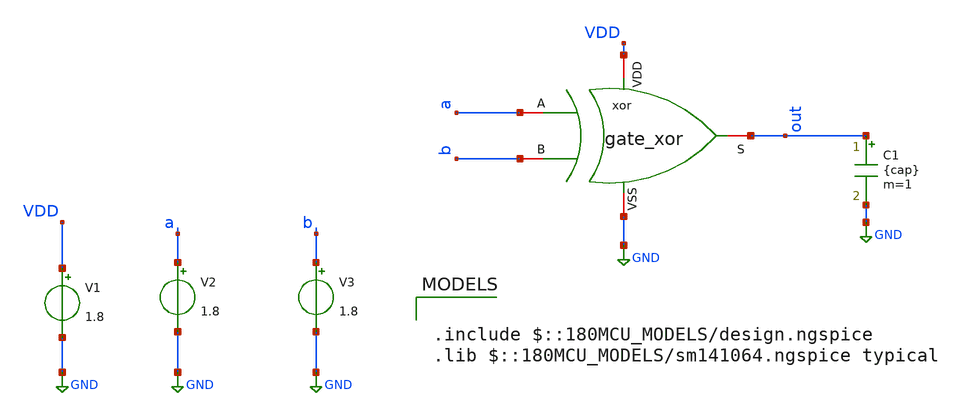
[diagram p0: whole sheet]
** sch_path: designs/DS_modulator/gate_xor/xschem/gate_xor_TB.sch
**.subckt gate_xor_TB
V1 VDD GND 1.8
V2 a GND 1.8
V3 b GND 1.8
xor VDD out a b GND gate_xor
C1 out GND {cap} m=1
**** begin user architecture code

.include $::180MCU_MODELS/design.ngspice
.lib $::180MCU_MODELS/sm141064.ngspice typical




.control
*------------------- Parámetros -------------------
.param wxor=5.6u
.param cap=5f

*------------------- Guardar nodos -------------------
save all

* Entradas A y B con pulsos desfasados
alter @v2[PULSE]=(0 1.8 0 10p 10p 2.5n 10n)   ; Señal A
alter @v3[PULSE]=(0 1.8 0 10p 10p 1.5n 5n)    ; Señal B

*------------------- Simulación -------------------
TRAN 0.01n 20n


plot v(A) v(B) v(out)


* Medidas para caracterización
.meas TRAN t_rise TRIG v(b)=0.9 RISE=1 TARG v(out)=0.9 RISE=1
.meas TRAN t_fall TRIG v(b)=0.9 FALL=1 TARG v(out)=0.9 FALL=1

* Guardar resultados
*write prueba_xor.raw
.endc


**** end user architecture code
**.ends

* expanding   symbol:  gf180/gate_xor/xschem/gate_xor.sym # of pins=5
** sym_path: designs/DS_modulator/gate_xor/xschem/gate_xor.sym
** sch_path: designs/DS_modulator/gate_xor/xschem/gate_xor.sch
.subckt gate_xor VDD S A B VSS
*.iopin VSS
*.iopin VDD
*.iopin S
*.iopin A
*.iopin B
XM2 S B vz VSS nfet_03v3 L=0.28u W=1u nf=1 ad='int((nf+1)/2) * W/nf * 0.18u' as='int((nf+2)/2) * W/nf * 0.18u'
+ pd='2*int((nf+1)/2) * (W/nf + 0.18u)' ps='2*int((nf+2)/2) * (W/nf + 0.18u)' nrd='0.18u / W' nrs='0.18u / W'
+ sa=0 sb=0 sd=0 m=4
XM3 S -B vx VDD pfet_03v3 L=0.28u W=3u nf=1 ad='int((nf+1)/2) * W/nf * 0.18u' as='int((nf+2)/2) * W/nf * 0.18u'
+ pd='2*int((nf+1)/2) * (W/nf + 0.18u)' ps='2*int((nf+2)/2) * (W/nf + 0.18u)' nrd='0.18u / W' nrs='0.18u / W'
+ sa=0 sb=0 sd=0 m=4
XM1 vx A VDD VDD pfet_03v3 L=0.28u W=3u nf=1 ad='int((nf+1)/2) * W/nf * 0.18u' as='int((nf+2)/2) * W/nf * 0.18u'
+ pd='2*int((nf+1)/2) * (W/nf + 0.18u)' ps='2*int((nf+2)/2) * (W/nf + 0.18u)' nrd='0.18u / W' nrs='0.18u / W'
+ sa=0 sb=0 sd=0 m=4
XM4 S -B vw VSS nfet_03v3 L=0.28u W=1u nf=1 ad='int((nf+1)/2) * W/nf * 0.18u' as='int((nf+2)/2) * W/nf * 0.18u'
+ pd='2*int((nf+1)/2) * (W/nf + 0.18u)' ps='2*int((nf+2)/2) * (W/nf + 0.18u)' nrd='0.18u / W' nrs='0.18u / W'
+ sa=0 sb=0 sd=0 m=4
XM5 S B vy VDD pfet_03v3 L=0.28u W=3u nf=1 ad='int((nf+1)/2) * W/nf * 0.18u' as='int((nf+2)/2) * W/nf * 0.18u'
+ pd='2*int((nf+1)/2) * (W/nf + 0.18u)' ps='2*int((nf+2)/2) * (W/nf + 0.18u)' nrd='0.18u / W' nrs='0.18u / W'
+ sa=0 sb=0 sd=0 m=4
XM6 vy -A VDD VDD pfet_03v3 L=0.28u W=3u nf=1 ad='int((nf+1)/2) * W/nf * 0.18u' as='int((nf+2)/2) * W/nf * 0.18u'
+ pd='2*int((nf+1)/2) * (W/nf + 0.18u)' ps='2*int((nf+2)/2) * (W/nf + 0.18u)' nrd='0.18u / W' nrs='0.18u / W'
+ sa=0 sb=0 sd=0 m=4
XM7 vz A VSS VSS nfet_03v3 L=0.28u W=1u nf=1 ad='int((nf+1)/2) * W/nf * 0.18u' as='int((nf+2)/2) * W/nf * 0.18u'
+ pd='2*int((nf+1)/2) * (W/nf + 0.18u)' ps='2*int((nf+2)/2) * (W/nf + 0.18u)' nrd='0.18u / W' nrs='0.18u / W'
+ sa=0 sb=0 sd=0 m=4
XM8 vw -A VSS VSS nfet_03v3 L=0.28u W=1u nf=1 ad='int((nf+1)/2) * W/nf * 0.18u' as='int((nf+2)/2) * W/nf * 0.18u'
+ pd='2*int((nf+1)/2) * (W/nf + 0.18u)' ps='2*int((nf+2)/2) * (W/nf + 0.18u)' nrd='0.18u / W' nrs='0.18u / W'
+ sa=0 sb=0 sd=0 m=4
xINVA VDD -A A VSS gate_inv_L0d28
xINVB VDD -B B VSS gate_inv_L0d28
XM10 VDD VDD vx VDD pfet_03v3 L=0.28u W=3u nf=1 ad='int((nf+1)/2) * W/nf * 0.18u' as='int((nf+2)/2) * W/nf * 0.18u'
+ pd='2*int((nf+1)/2) * (W/nf + 0.18u)' ps='2*int((nf+2)/2) * (W/nf + 0.18u)' nrd='0.18u / W' nrs='0.18u / W'
+ sa=0 sb=0 sd=0 m=2
XM11 VDD VDD vy VDD pfet_03v3 L=0.28u W=3u nf=1 ad='int((nf+1)/2) * W/nf * 0.18u' as='int((nf+2)/2) * W/nf * 0.18u'
+ pd='2*int((nf+1)/2) * (W/nf + 0.18u)' ps='2*int((nf+2)/2) * (W/nf + 0.18u)' nrd='0.18u / W' nrs='0.18u / W'
+ sa=0 sb=0 sd=0 m=2
XM13 vz VSS VSS VSS nfet_03v3 L=0.28u W=1u nf=1 ad='int((nf+1)/2) * W/nf * 0.18u' as='int((nf+2)/2) * W/nf * 0.18u'
+ pd='2*int((nf+1)/2) * (W/nf + 0.18u)' ps='2*int((nf+2)/2) * (W/nf + 0.18u)' nrd='0.18u / W' nrs='0.18u / W'
+ sa=0 sb=0 sd=0 m=2
XM14 vw VSS VSS VSS nfet_03v3 L=0.28u W=1u nf=1 ad='int((nf+1)/2) * W/nf * 0.18u' as='int((nf+2)/2) * W/nf * 0.18u'
+ pd='2*int((nf+1)/2) * (W/nf + 0.18u)' ps='2*int((nf+2)/2) * (W/nf + 0.18u)' nrd='0.18u / W' nrs='0.18u / W'
+ sa=0 sb=0 sd=0 m=2
.ends


* expanding   symbol:
*+  /foss/designs/chipathon_2025/designs/gf180/gate_inv_L0d28/xschem/gate_inv_L0d28.sym # of pins=4
** sym_path: designs/DS_modulator/gate_inv_L0d28/xschem/gate_inv_L0d28.sym
** sch_path: designs/DS_modulator/gate_inv_L0d28/xschem/gate_inv_L0d28.sch
.subckt gate_inv_L0d28 VDD B A VSS
*.opin B
*.ipin A
*.iopin VDD
*.iopin VSS
XMN B A VSS VSS nfet_03v3 L=0.28u W=1u nf=1 ad='int((nf+1)/2) * W/nf * 0.18u' as='int((nf+2)/2) * W/nf * 0.18u'
+ pd='2*int((nf+1)/2) * (W/nf + 0.18u)' ps='2*int((nf+2)/2) * (W/nf + 0.18u)' nrd='0.18u / W' nrs='0.18u / W'
+ sa=0 sb=0 sd=0 m=2
XMP B A VDD VDD pfet_03v3 L=0.28u W=3u nf=1 ad='int((nf+1)/2) * W/nf * 0.18u' as='int((nf+2)/2) * W/nf * 0.18u'
+ pd='2*int((nf+1)/2) * (W/nf + 0.18u)' ps='2*int((nf+2)/2) * (W/nf + 0.18u)' nrd='0.18u / W' nrs='0.18u / W'
+ sa=0 sb=0 sd=0 m=2
.ends

.GLOBAL GND
.end
